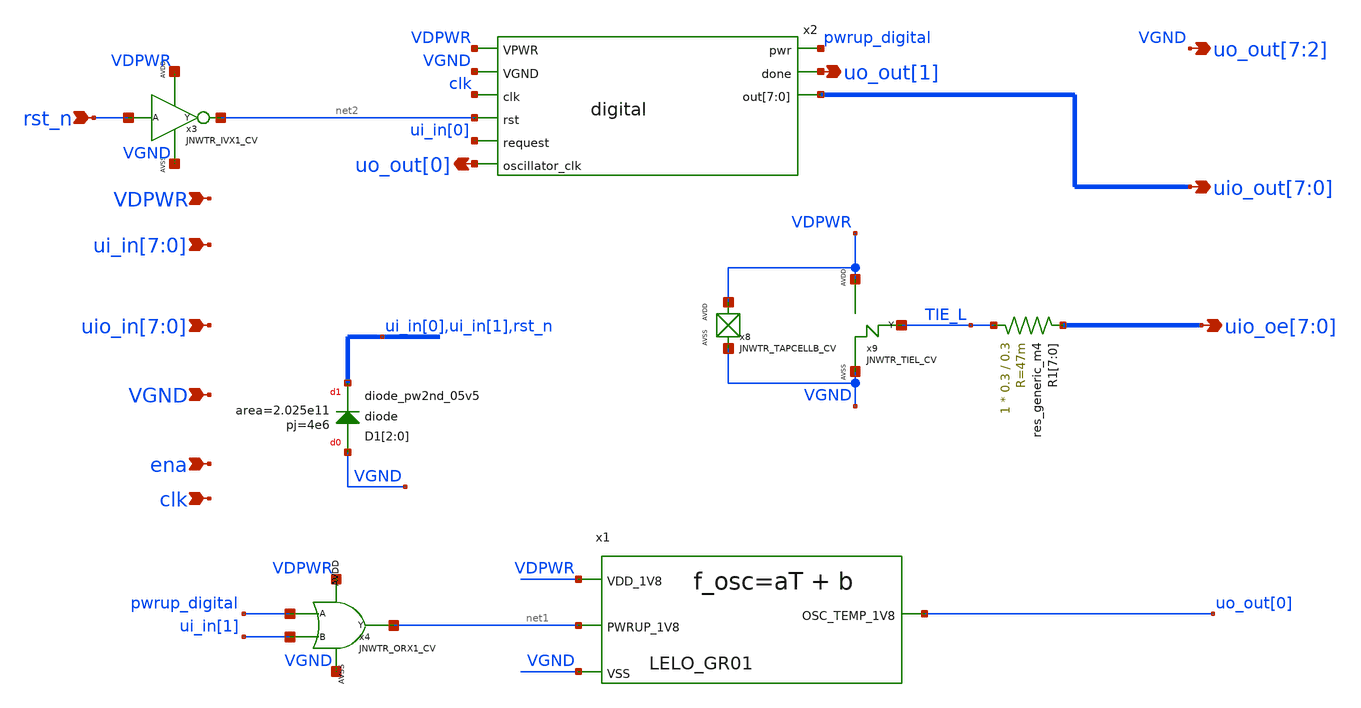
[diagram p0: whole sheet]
** sch_path: design/LELO_GR01_SKY130A/tt_um_lelo_gr01_analogicus.sch
**.subckt tt_um_lelo_gr01_analogicus uo_out[7],uo_out[6],uo_out[5],uo_out[4],uo_out[3],uo_out[2]
*+ uio_out[7],uio_out[6],uio_out[5],uio_out[4],uio_out[3],uio_out[2],uio_out[1],uio_out[0] uio_oe[7],uio_oe[6],uio_oe[5],uio_oe[4],uio_oe[3],uio_oe[2],uio_oe[1],uio_oe[0] VDPWR VGND
*+ ui_in[7],ui_in[6],ui_in[5],ui_in[4],ui_in[3],ui_in[2],ui_in[1],ui_in[0] uio_in[7],uio_in[6],uio_in[5],uio_in[4],uio_in[3],uio_in[2],uio_in[1],uio_in[0] ena rst_n clk
*+ uo_out[0] uo_out[1]
*.opin uo_out[7],uo_out[6],uo_out[5],uo_out[4],uo_out[3],uo_out[2]
*.opin uio_out[7],uio_out[6],uio_out[5],uio_out[4],uio_out[3],uio_out[2],uio_out[1],uio_out[0]
*.opin uio_oe[7],uio_oe[6],uio_oe[5],uio_oe[4],uio_oe[3],uio_oe[2],uio_oe[1],uio_oe[0]
*.ipin VDPWR
*.ipin VGND
*.ipin ui_in[7],ui_in[6],ui_in[5],ui_in[4],ui_in[3],ui_in[2],ui_in[1],ui_in[0]
*.ipin uio_in[7],uio_in[6],uio_in[5],uio_in[4],uio_in[3],uio_in[2],uio_in[1],uio_in[0]
*.ipin ena
*.ipin rst_n
*.ipin clk
*.opin uo_out[0]
*.opin uo_out[1]
x8 VDPWR VGND JNWTR_TAPCELLB_CV xoffset=0 yoffset=0 angle=0
R1[7] TIE_L uio_oe[7] sky130_fd_pr__res_generic_m4 W=0.3 L=0.3 m=1
R1[6] TIE_L uio_oe[6] sky130_fd_pr__res_generic_m4 W=0.3 L=0.3 m=1
R1[5] TIE_L uio_oe[5] sky130_fd_pr__res_generic_m4 W=0.3 L=0.3 m=1
R1[4] TIE_L uio_oe[4] sky130_fd_pr__res_generic_m4 W=0.3 L=0.3 m=1
R1[3] TIE_L uio_oe[3] sky130_fd_pr__res_generic_m4 W=0.3 L=0.3 m=1
R1[2] TIE_L uio_oe[2] sky130_fd_pr__res_generic_m4 W=0.3 L=0.3 m=1
R1[1] TIE_L uio_oe[1] sky130_fd_pr__res_generic_m4 W=0.3 L=0.3 m=1
R1[0] TIE_L uio_oe[0] sky130_fd_pr__res_generic_m4 W=0.3 L=0.3 m=1
x1 VDPWR uo_out[0] net1 VGND LELO_GR01
x2 VDPWR VGND clk pwrup_digital net2 uo_out[1] ui_in[0] uio_out[7] uio_out[6] uio_out[5] uio_out[4]
+ uio_out[3] uio_out[2] uio_out[1] uio_out[0] uo_out[0] digital
x3 rst_n net2 VDPWR VGND JNWTR_IVX1_CV
x4 pwrup_digital ui_in[1] net1 VDPWR VGND JNWTR_ORX1_CV xoffset=0 yoffset=0 angle=0 M=1
XD1[2] VGND ui_in[0] sky130_fd_pr__diode_pw2nd_05v5 area=2.025e11 pj=4e6
XD1[1] VGND ui_in[1] sky130_fd_pr__diode_pw2nd_05v5 area=2.025e11 pj=4e6
XD1[0] VGND rst_n sky130_fd_pr__diode_pw2nd_05v5 area=2.025e11 pj=4e6
**.ends
.end
